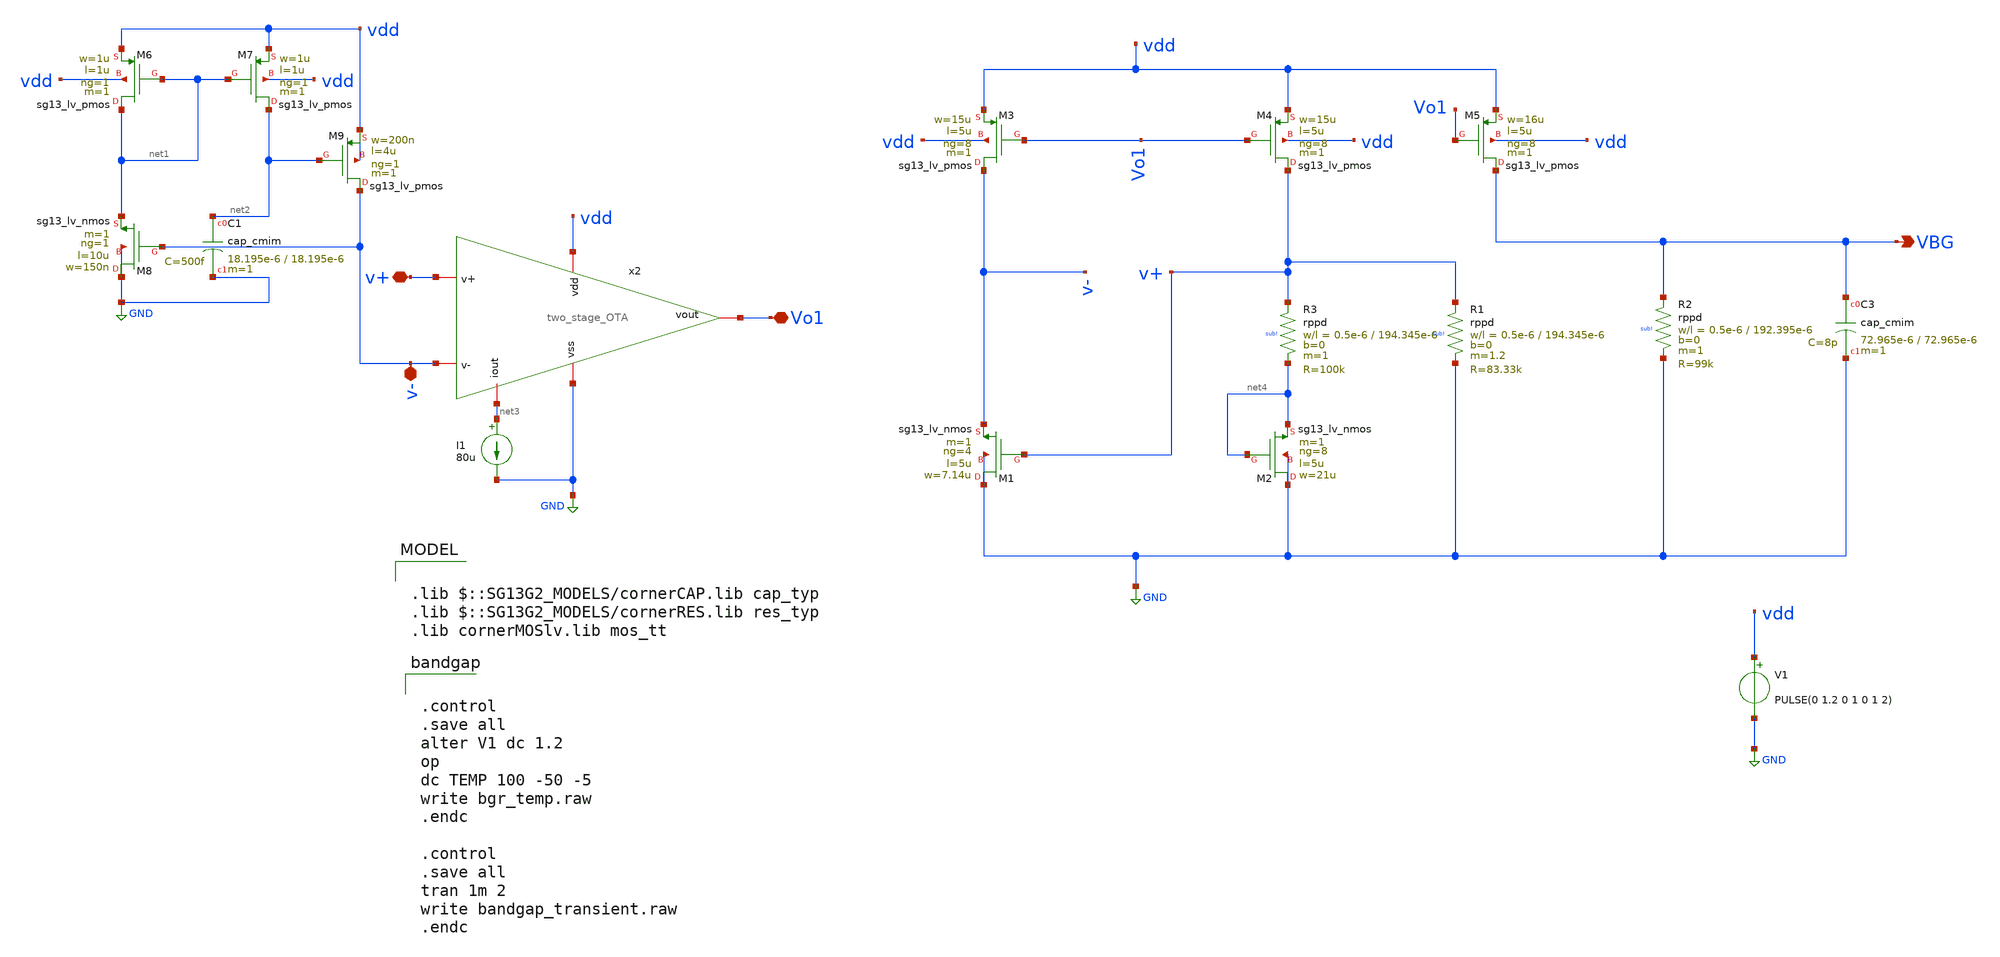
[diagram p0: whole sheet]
** sch_path: modules/module_1_bandgap_reference/part_2_full_bgr/schematic/bandgap_reference.sch
**.subckt bandgap_reference v+ v- Vo1 VBG
*.iopin v+
*.iopin v-
*.iopin Vo1
*.opin VBG
XM8 GND v- net1 GND sg13_lv_nmos w=150n l=10u ng=1 m=1 mm_ok=1
XM6 net1 net1 vdd vdd sg13_lv_pmos w=1u l=1u ng=1 m=1 mm_ok=1
XM7 net2 net1 vdd vdd sg13_lv_pmos w=1u l=1u ng=1 m=1 mm_ok=1
XM9 v- net2 vdd vdd sg13_lv_pmos w=200n l=4u ng=1 m=1 mm_ok=1
x2 vdd net3 v+ v- Vo1 GND two_stage_OTA
I1 net3 GND 80u
V1 vdd GND PULSE(0 1.2 0 1 0 1 2)
XM1 GND v+ v- GND sg13_lv_nmos w=7.14u l=5u ng=4 m=1 mm_ok=1
XM2 GND net4 net4 GND sg13_lv_nmos w=21u l=5u ng=8 m=1 mm_ok=1
XM3 v- Vo1 vdd vdd sg13_lv_pmos w=15u l=5u ng=8 m=1 mm_ok=1
XM4 v+ Vo1 vdd vdd sg13_lv_pmos w=15u l=5u ng=8 m=1 mm_ok=1
XM5 VBG Vo1 vdd vdd sg13_lv_pmos w=16u l=5u ng=8 m=1 mm_ok=1
XC3 VBG GND cap_cmim w=72.965e-6 l=72.965e-6 m=1 mm_ok=1
XR3 v+ net4 sub! rppd w=0.5e-6 l=194.345e-6 m=1 b=0 mm_ok=1
XR1 v+ GND sub! rppd w=0.5e-6 l=194.345e-6 m=1.2 b=0 mm_ok=1
XR2 VBG GND sub! rppd w=0.5e-6 l=192.395e-6 m=1 b=0 mm_ok=1
XC1 net2 GND cap_cmim w=18.195e-6 l=18.195e-6 m=1 mm_ok=1
**** begin user architecture code


.control
.save all
alter V1 dc 1.2
op
dc TEMP 100 -50 -5
write bgr_temp.raw
.endc

.control
.save all
tran 1m 2
write bandgap_transient.raw
.endc



.lib $::SG13G2_MODELS/cornerCAP.lib cap_typ
.lib $::SG13G2_MODELS/cornerRES.lib res_typ
.lib cornerMOSlv.lib mos_tt

**** end user architecture code
**.ends

* expanding   symbol:
*+  /home/pedersen/projects/IHP-AnalogAcademy/modules/module_1_bandgap_reference/part_1_OTA/schematic/two_stage_OTA.sym # of pins=6
** sym_path: /home/pedersen/projects/IHP-AnalogAcademy/modules/module_1_bandgap_reference/part_1_OTA/schematic/two_stage_OTA.sym
** sch_path: /home/pedersen/projects/IHP-AnalogAcademy/modules/module_1_bandgap_reference/part_1_OTA/schematic/two_stage_OTA.sch
.subckt two_stage_OTA vdd iout v+ v- vout vss
*.iopin v-
*.iopin v+
*.iopin vss
*.iopin vdd
*.iopin iout
*.iopin vout
XM4 vss net1 net3 vss sg13_lv_nmos w=720n l=9.75u ng=1 m=1 mm_ok=1
XM3 vss net1 net1 vss sg13_lv_nmos w=720n l=9.75u ng=1 m=1 mm_ok=1
XM1 net1 v- net2 vdd sg13_lv_pmos w=7.41u l=3.64u ng=1 m=1 mm_ok=1
XM2 net3 v+ net2 vdd sg13_lv_pmos w=7.41u l=3.64u ng=1 m=1 mm_ok=1
XM5 net2 iout vdd vdd sg13_lv_pmos w=5.3u l=1.95u ng=1 m=1 mm_ok=1
XM7 vout iout vdd vdd sg13_lv_pmos w=75u l=2.08u ng=8 m=1 mm_ok=1
XM6 vss net3 vout vss sg13_lv_nmos w=28.8u l=9.75u ng=4 m=1 mm_ok=1
XM9 iout iout vdd vdd sg13_lv_pmos w=75u l=2.08u ng=8 m=1 mm_ok=1
XC2 net3 vout cap_cmim w=22.295e-6 l=22.295e-6 m=1 mm_ok=1
.ends

.GLOBAL GND
.end
